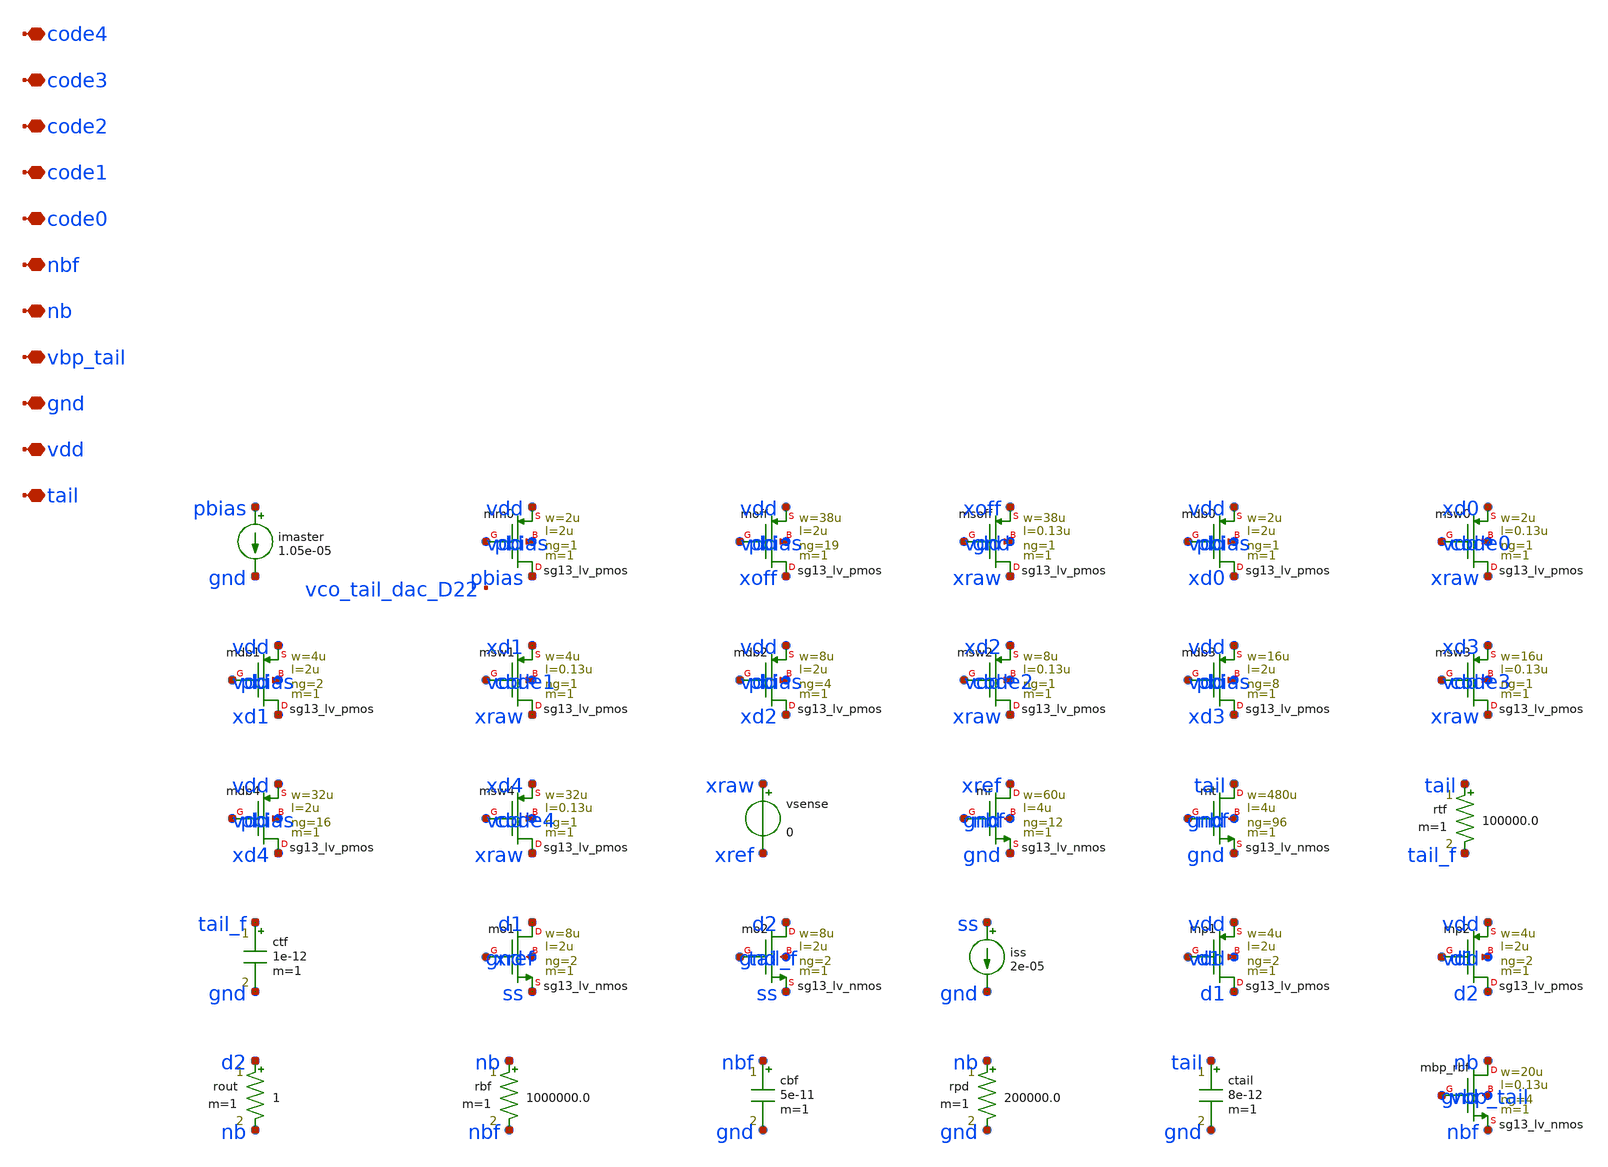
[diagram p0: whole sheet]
** sch_path: analog/vco/sch/vco_tail_dac.sch
**.subckt vco_tail_dac tail vdd gnd vbp_tail nb nbf code0 code1 code2 code3 code4
*.iopin tail
*.iopin vdd
*.iopin gnd
*.iopin vbp_tail
*.iopin nb
*.iopin nbf
*.iopin code0
*.iopin code1
*.iopin code2
*.iopin code3
*.iopin code4
imaster pbias gnd 1.05e-05
Xmm0 pbias pbias vdd vdd sg13_lv_pmos w=2u l=2u ng=1 m=1 mm_ok=1
Xmoff xoff pbias vdd vdd sg13_lv_pmos w=38u l=2u ng=19 m=1 mm_ok=1
Xmsoff xraw gnd xoff vdd sg13_lv_pmos w=38u l=0.13u ng=1 m=1 mm_ok=1
Xmdb0 xd0 pbias vdd vdd sg13_lv_pmos w=2u l=2u ng=1 m=1 mm_ok=1
Xmsw0 xraw code0 xd0 vdd sg13_lv_pmos w=2u l=0.13u ng=1 m=1 mm_ok=1
Xmdb1 xd1 pbias vdd vdd sg13_lv_pmos w=4u l=2u ng=2 m=1 mm_ok=1
Xmsw1 xraw code1 xd1 vdd sg13_lv_pmos w=4u l=0.13u ng=1 m=1 mm_ok=1
Xmdb2 xd2 pbias vdd vdd sg13_lv_pmos w=8u l=2u ng=4 m=1 mm_ok=1
Xmsw2 xraw code2 xd2 vdd sg13_lv_pmos w=8u l=0.13u ng=1 m=1 mm_ok=1
Xmdb3 xd3 pbias vdd vdd sg13_lv_pmos w=16u l=2u ng=8 m=1 mm_ok=1
Xmsw3 xraw code3 xd3 vdd sg13_lv_pmos w=16u l=0.13u ng=1 m=1 mm_ok=1
Xmdb4 xd4 pbias vdd vdd sg13_lv_pmos w=32u l=2u ng=16 m=1 mm_ok=1
Xmsw4 xraw code4 xd4 vdd sg13_lv_pmos w=32u l=0.13u ng=1 m=1 mm_ok=1
vsense xraw xref 0
Xmr xref nbf gnd gnd sg13_lv_nmos w=60u l=4u ng=12 m=1 mm_ok=1
Xmt tail nbf gnd gnd sg13_lv_nmos w=480u l=4u ng=96 m=1 mm_ok=1
rtf tail tail_f 100000.0 m=1
ctf tail_f gnd 1e-12 m=1
Xmo1 d1 xref ss gnd sg13_lv_nmos w=8u l=2u ng=2 m=1 mm_ok=1
Xmo2 d2 tail_f ss gnd sg13_lv_nmos w=8u l=2u ng=2 m=1 mm_ok=1
iss ss gnd 2e-05
Xmp1 d1 d1 vdd vdd sg13_lv_pmos w=4u l=2u ng=2 m=1 mm_ok=1
Xmp2 d2 d1 vdd vdd sg13_lv_pmos w=4u l=2u ng=2 m=1 mm_ok=1
rout d2 nb 1 m=1
rbf nb nbf 1000000.0 m=1
cbf nbf gnd 5e-11 m=1
rpd nb gnd 200000.0 m=1
ctail tail gnd 8e-12 m=1
Xmbp_rbf nb vbp_tail nbf gnd sg13_lv_nmos w=20u l=0.13u ng=4 m=1 mm_ok=1
**.ends
.end
